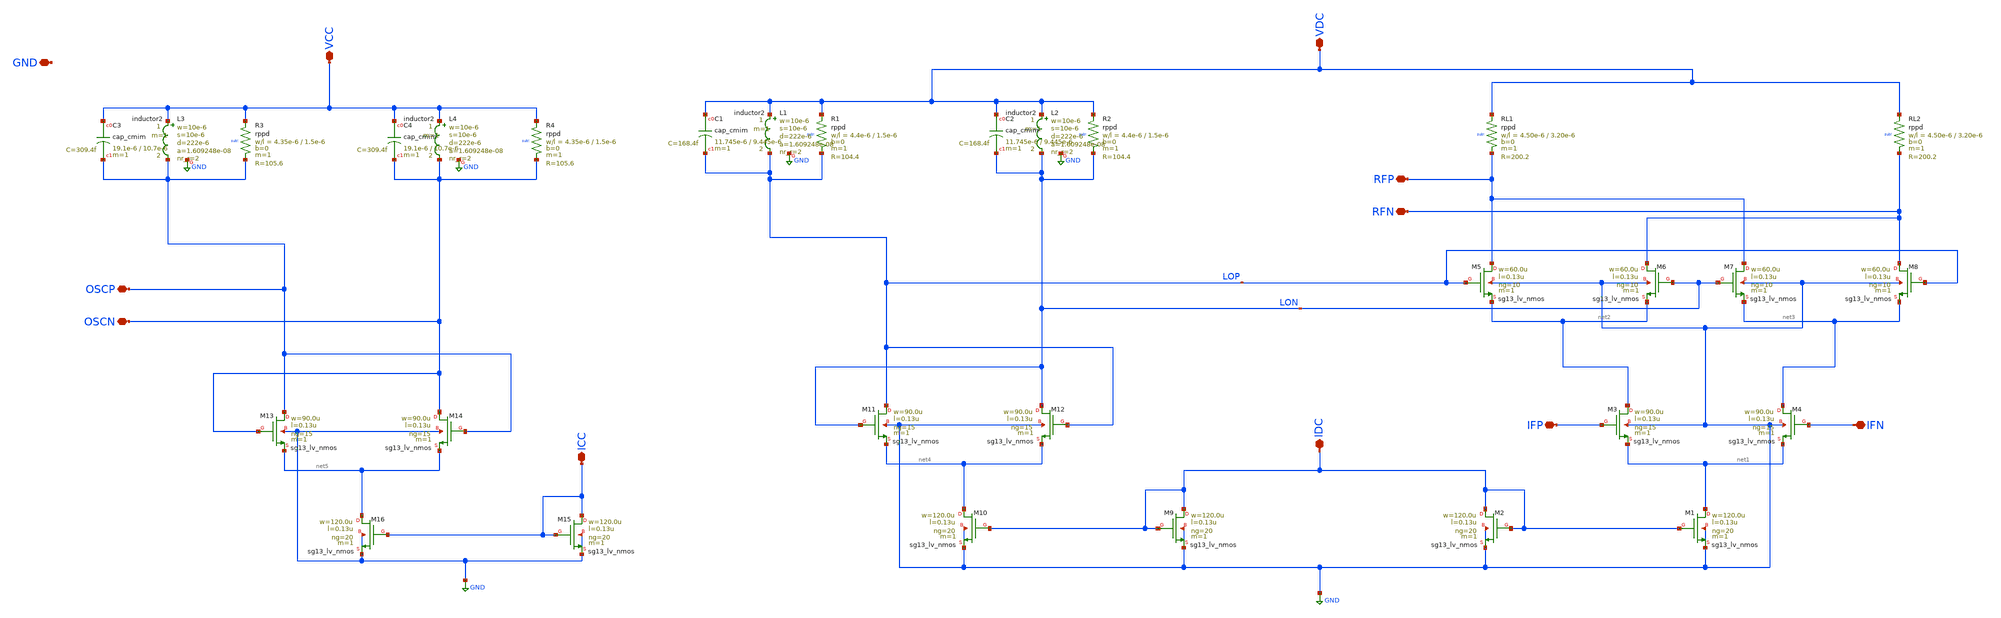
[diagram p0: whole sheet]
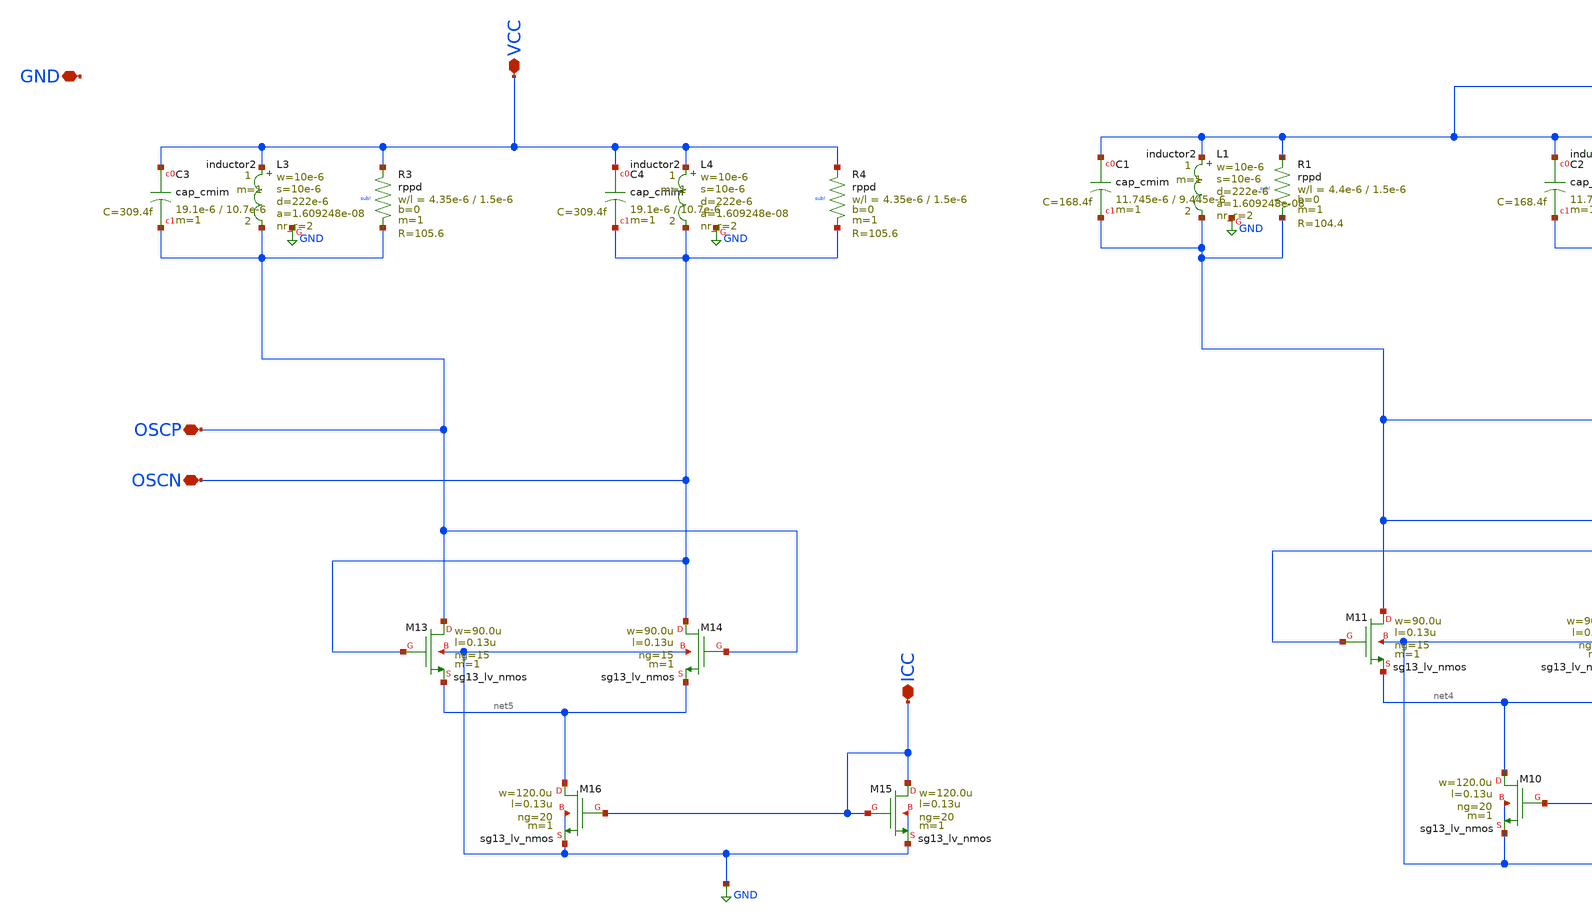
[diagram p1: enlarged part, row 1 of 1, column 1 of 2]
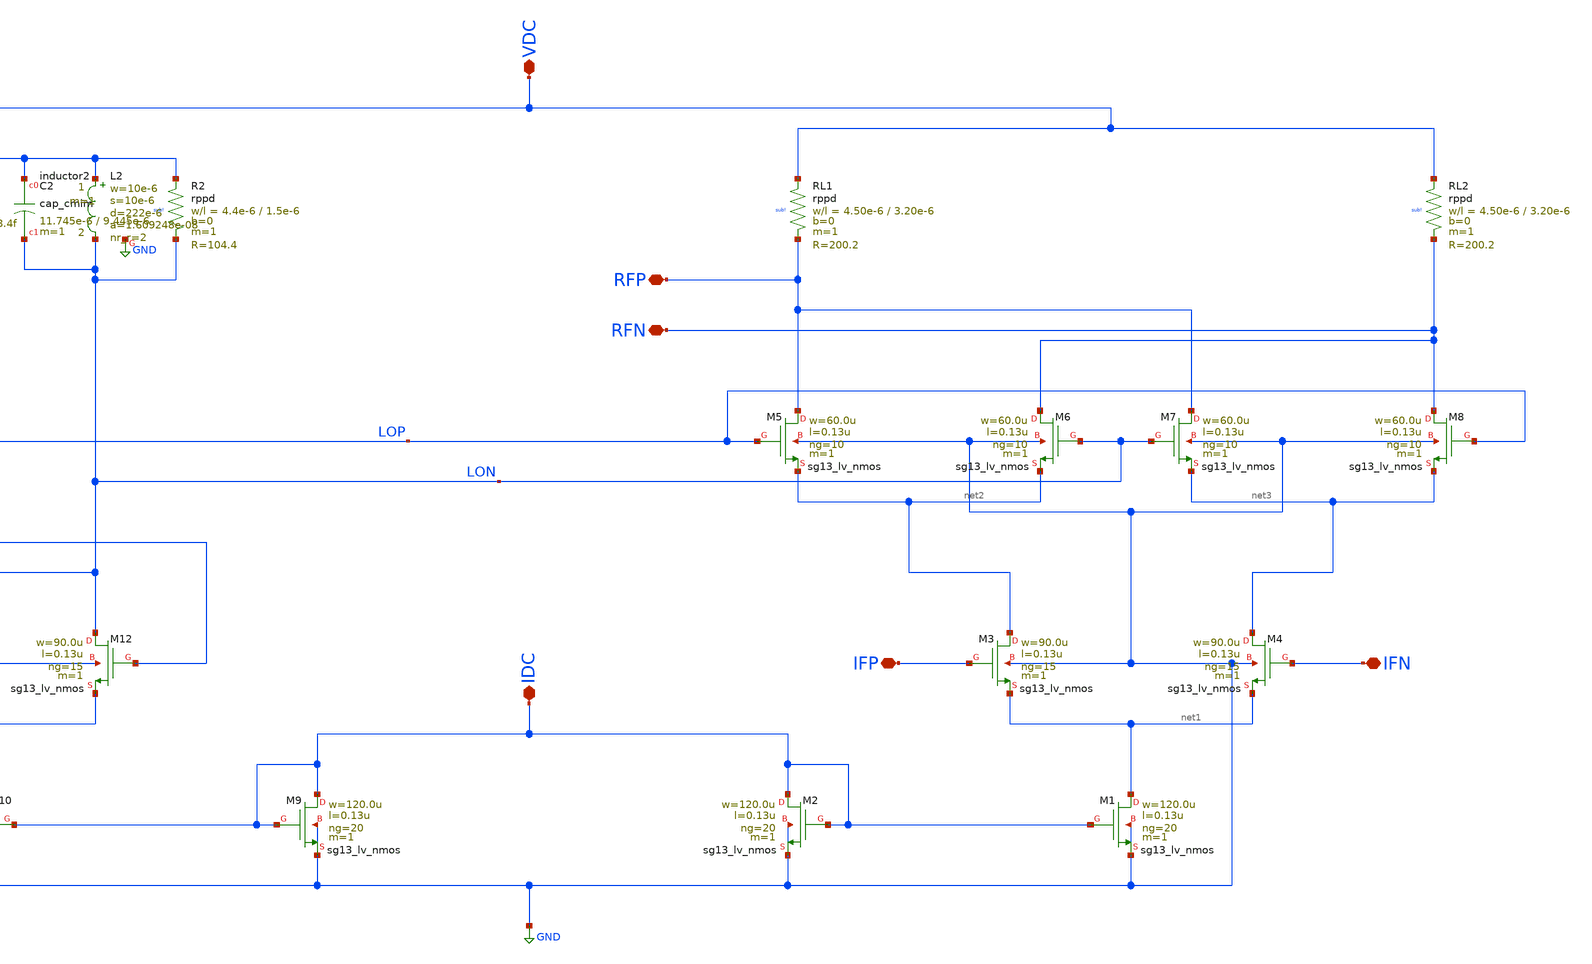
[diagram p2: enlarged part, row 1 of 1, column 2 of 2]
** sch_path: TO_Apr2025/Mixer5GHz/xschem/Mixer5GHz.sch
**.subckt Mixer5GHz RFN RFP VDC IFP IFN IDC OSCN OSCP VCC ICC GND
*.iopin RFN
*.iopin RFP
*.iopin VDC
*.iopin IFP
*.iopin IFN
*.iopin IDC
*.iopin OSCN
*.iopin OSCP
*.iopin VCC
*.iopin ICC
*.iopin GND
XM6 RFN LON net2 GND sg13_lv_nmos w=60.0u l=0.13u ng=10 m=1 mm_ok=1
XRL2 VDC RFN sub! rppd w=4.50e-6 l=3.20e-6 m=1 b=0 mm_ok=1
XRL1 VDC RFP sub! rppd w=4.50e-6 l=3.20e-6 m=1 b=0 mm_ok=1
XM8 RFN LOP net3 GND sg13_lv_nmos w=60.0u l=0.13u ng=10 m=1 mm_ok=1
XM7 RFP LON net3 GND sg13_lv_nmos w=60.0u l=0.13u ng=10 m=1 mm_ok=1
XM5 RFP LOP net2 GND sg13_lv_nmos w=60.0u l=0.13u ng=10 m=1 mm_ok=1
XM4 net3 IFN net1 GND sg13_lv_nmos w=90.0u l=0.13u ng=15 m=1 mm_ok=1
XM3 net2 IFP net1 GND sg13_lv_nmos w=90.0u l=0.13u ng=15 m=1 mm_ok=1
XM2 IDC IDC GND GND sg13_lv_nmos w=120.0u l=0.13u ng=20 m=1 mm_ok=1
XM1 net1 IDC GND GND sg13_lv_nmos w=120.0u l=0.13u ng=20 m=1 mm_ok=1
XM11 LOP LON net4 GND sg13_lv_nmos w=90.0u l=0.13u ng=15 m=1 mm_ok=1
XM12 LON LOP net4 GND sg13_lv_nmos w=90.0u l=0.13u ng=15 m=1 mm_ok=1
XM9 IDC IDC GND GND sg13_lv_nmos w=120.0u l=0.13u ng=20 m=1 mm_ok=1
XM10 net4 IDC GND GND sg13_lv_nmos w=120.0u l=0.13u ng=20 m=1 mm_ok=1
XC1 VDC LOP cap_cmim w=11.745e-6 l=9.445e-6 m=1 mm_ok=1
XR1 VDC LOP sub! rppd w=4.4e-6 l=1.5e-6 m=1 b=0 mm_ok=1
XC2 VDC LON cap_cmim w=11.745e-6 l=9.445e-6 m=1 mm_ok=1
XR2 VDC LON sub! rppd w=4.4e-6 l=1.5e-6 m=1 b=0 mm_ok=1
XM13 OSCP OSCN net5 GND sg13_lv_nmos w=90.0u l=0.13u ng=15 m=1 mm_ok=1
XM14 OSCN OSCP net5 GND sg13_lv_nmos w=90.0u l=0.13u ng=15 m=1 mm_ok=1
XM15 ICC ICC GND GND sg13_lv_nmos w=120.0u l=0.13u ng=20 m=1 mm_ok=1
XM16 net5 ICC GND GND sg13_lv_nmos w=120.0u l=0.13u ng=20 m=1 mm_ok=1
XC3 VCC OSCP cap_cmim w=19.1e-6 l=10.7e-6 m=1 mm_ok=1
XR3 VCC OSCP sub! rppd w=4.35e-6 l=1.5e-6 m=1 b=0 mm_ok=1
XC4 VCC OSCN cap_cmim w=19.1e-6 l=10.7e-6 m=1 mm_ok=1
XR4 VCC OSCN sub! rppd w=4.35e-6 l=1.5e-6 m=1 b=0 mm_ok=1
XL1 VDC LOP GND inductor2 w=10e-6 s=10e-6 d=222e-6 nr_r=2 m=1
XL2 VDC LON GND inductor2 w=10e-6 s=10e-6 d=222e-6 nr_r=2 m=1
XL3 VCC OSCP GND inductor2 w=10e-6 s=10e-6 d=222e-6 nr_r=2 m=1
XL4 VCC OSCN GND inductor2 w=10e-6 s=10e-6 d=222e-6 nr_r=2 m=1
**.ends
.end
